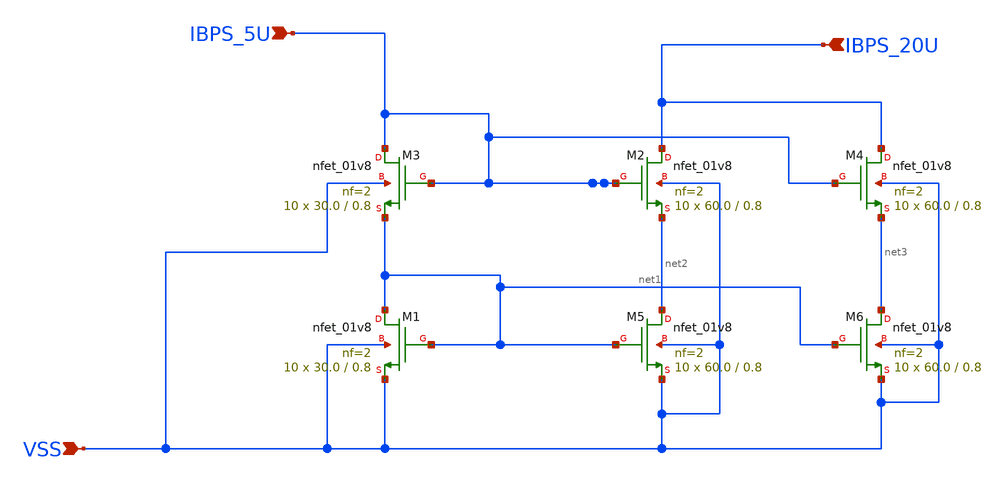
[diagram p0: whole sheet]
** sch_path: lelo_ex_sky130a/design/LELO_EX_SKY130A/LELO_EX.sch
**.subckt LELO_EX IBPS_5U VSS IBPS_20U
*.ipin IBPS_5U
*.ipin VSS
*.ipin IBPS_20U
XM1 net1 net1 VSS VSS sky130_fd_pr__nfet_01v8 L=0.8 W=30.0 nf=2 ad='int((2 + 1)/2) * 30.0 / 2 * 0.29'
+ as='int((2 + 2)/2) * 30.0 / 2 * 0.29' pd='2*int((2 + 1)/2) * (30.0 / 2 + 0.29)' ps='2*int((2 + 2)/2) * (30.0 / 2 + 0.29)'
+ nrd='0.29 / 30.0 ' nrs='0.29 / 30.0 ' sa=0 sb=0 sd=0 mult=10 m=10
XM2 IBPS_20U IBPS_5U net2 VSS sky130_fd_pr__nfet_01v8 L=0.8 W=60.0 nf=2 ad='int((2 + 1)/2) * 60.0 / 2 * 0.29'
+ as='int((2 + 2)/2) * 60.0 / 2 * 0.29' pd='2*int((2 + 1)/2) * (60.0 / 2 + 0.29)' ps='2*int((2 + 2)/2) * (60.0 / 2 + 0.29)'
+ nrd='0.29 / 60.0 ' nrs='0.29 / 60.0 ' sa=0 sb=0 sd=0 mult=10 m=10
XM3 IBPS_5U IBPS_5U net1 VSS sky130_fd_pr__nfet_01v8 L=0.8 W=30.0 nf=2 ad='int((2 + 1)/2) * 30.0 / 2 * 0.29'
+ as='int((2 + 2)/2) * 30.0 / 2 * 0.29' pd='2*int((2 + 1)/2) * (30.0 / 2 + 0.29)' ps='2*int((2 + 2)/2) * (30.0 / 2 + 0.29)'
+ nrd='0.29 / 30.0 ' nrs='0.29 / 30.0 ' sa=0 sb=0 sd=0 mult=10 m=10
XM4 IBPS_20U IBPS_5U net3 VSS sky130_fd_pr__nfet_01v8 L=0.8 W=60.0 nf=2 ad='int((2 + 1)/2) * 60.0 / 2 * 0.29'
+ as='int((2 + 2)/2) * 60.0 / 2 * 0.29' pd='2*int((2 + 1)/2) * (60.0 / 2 + 0.29)' ps='2*int((2 + 2)/2) * (60.0 / 2 + 0.29)'
+ nrd='0.29 / 60.0 ' nrs='0.29 / 60.0 ' sa=0 sb=0 sd=0 mult=10 m=10
XM5 net2 net1 VSS VSS sky130_fd_pr__nfet_01v8 L=0.8 W=60.0 nf=2 ad='int((2 + 1)/2) * 60.0 / 2 * 0.29'
+ as='int((2 + 2)/2) * 60.0 / 2 * 0.29' pd='2*int((2 + 1)/2) * (60.0 / 2 + 0.29)' ps='2*int((2 + 2)/2) * (60.0 / 2 + 0.29)'
+ nrd='0.29 / 60.0 ' nrs='0.29 / 60.0 ' sa=0 sb=0 sd=0 mult=10 m=10
XM6 net3 net1 VSS VSS sky130_fd_pr__nfet_01v8 L=0.8 W=60.0 nf=2 ad='int((2 + 1)/2) * 60.0 / 2 * 0.29'
+ as='int((2 + 2)/2) * 60.0 / 2 * 0.29' pd='2*int((2 + 1)/2) * (60.0 / 2 + 0.29)' ps='2*int((2 + 2)/2) * (60.0 / 2 + 0.29)'
+ nrd='0.29 / 60.0 ' nrs='0.29 / 60.0 ' sa=0 sb=0 sd=0 mult=10 m=10
**.ends
.end
